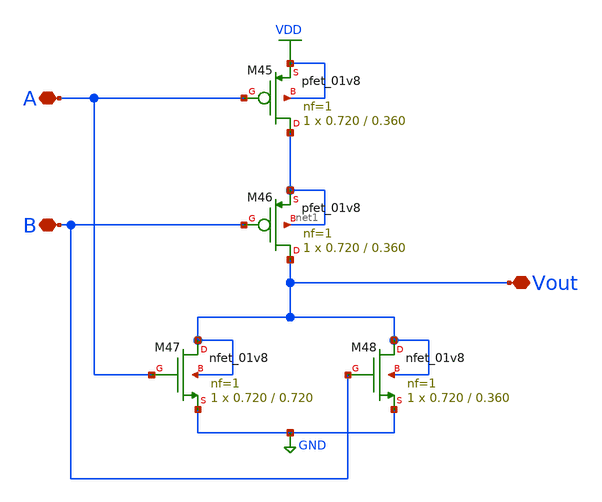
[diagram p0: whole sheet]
** sch_path: xschem/NOR_Gate.sch
**.subckt NOR_Gate Vout A B
*.iopin Vout
*.iopin A
*.iopin B
XM45 net1 A VDD VDD sky130_fd_pr__pfet_01v8 L=0.360 W=0.720 nf=1 ad='int((nf+1)/2) * W/nf * 0.29' as='int((nf+2)/2) * W/nf * 0.29'
+ pd='2*int((nf+1)/2) * (W/nf + 0.29)' ps='2*int((nf+2)/2) * (W/nf + 0.29)' nrd='0.29 / W' nrs='0.29 / W'
+ sa=0 sb=0 sd=0 mult=1 m=1
XM46 Vout B net1 net1 sky130_fd_pr__pfet_01v8 L=0.360 W=0.720 nf=1 ad='int((nf+1)/2) * W/nf * 0.29' as='int((nf+2)/2) * W/nf * 0.29'
+ pd='2*int((nf+1)/2) * (W/nf + 0.29)' ps='2*int((nf+2)/2) * (W/nf + 0.29)' nrd='0.29 / W' nrs='0.29 / W'
+ sa=0 sb=0 sd=0 mult=1 m=1
XM47 Vout A GND Vout sky130_fd_pr__nfet_01v8 L=0.720 W=0.720 nf=1 ad='int((nf+1)/2) * W/nf * 0.29' as='int((nf+2)/2) * W/nf * 0.29'
+ pd='2*int((nf+1)/2) * (W/nf + 0.29)' ps='2*int((nf+2)/2) * (W/nf + 0.29)' nrd='0.29 / W' nrs='0.29 / W'
+ sa=0 sb=0 sd=0 mult=1 m=1
XM48 Vout B GND Vout sky130_fd_pr__nfet_01v8 L=0.360 W=0.720 nf=1 ad='int((nf+1)/2) * W/nf * 0.29' as='int((nf+2)/2) * W/nf * 0.29'
+ pd='2*int((nf+1)/2) * (W/nf + 0.29)' ps='2*int((nf+2)/2) * (W/nf + 0.29)' nrd='0.29 / W' nrs='0.29 / W'
+ sa=0 sb=0 sd=0 mult=1 m=1
**.ends
.GLOBAL VDD
.GLOBAL GND
.end
